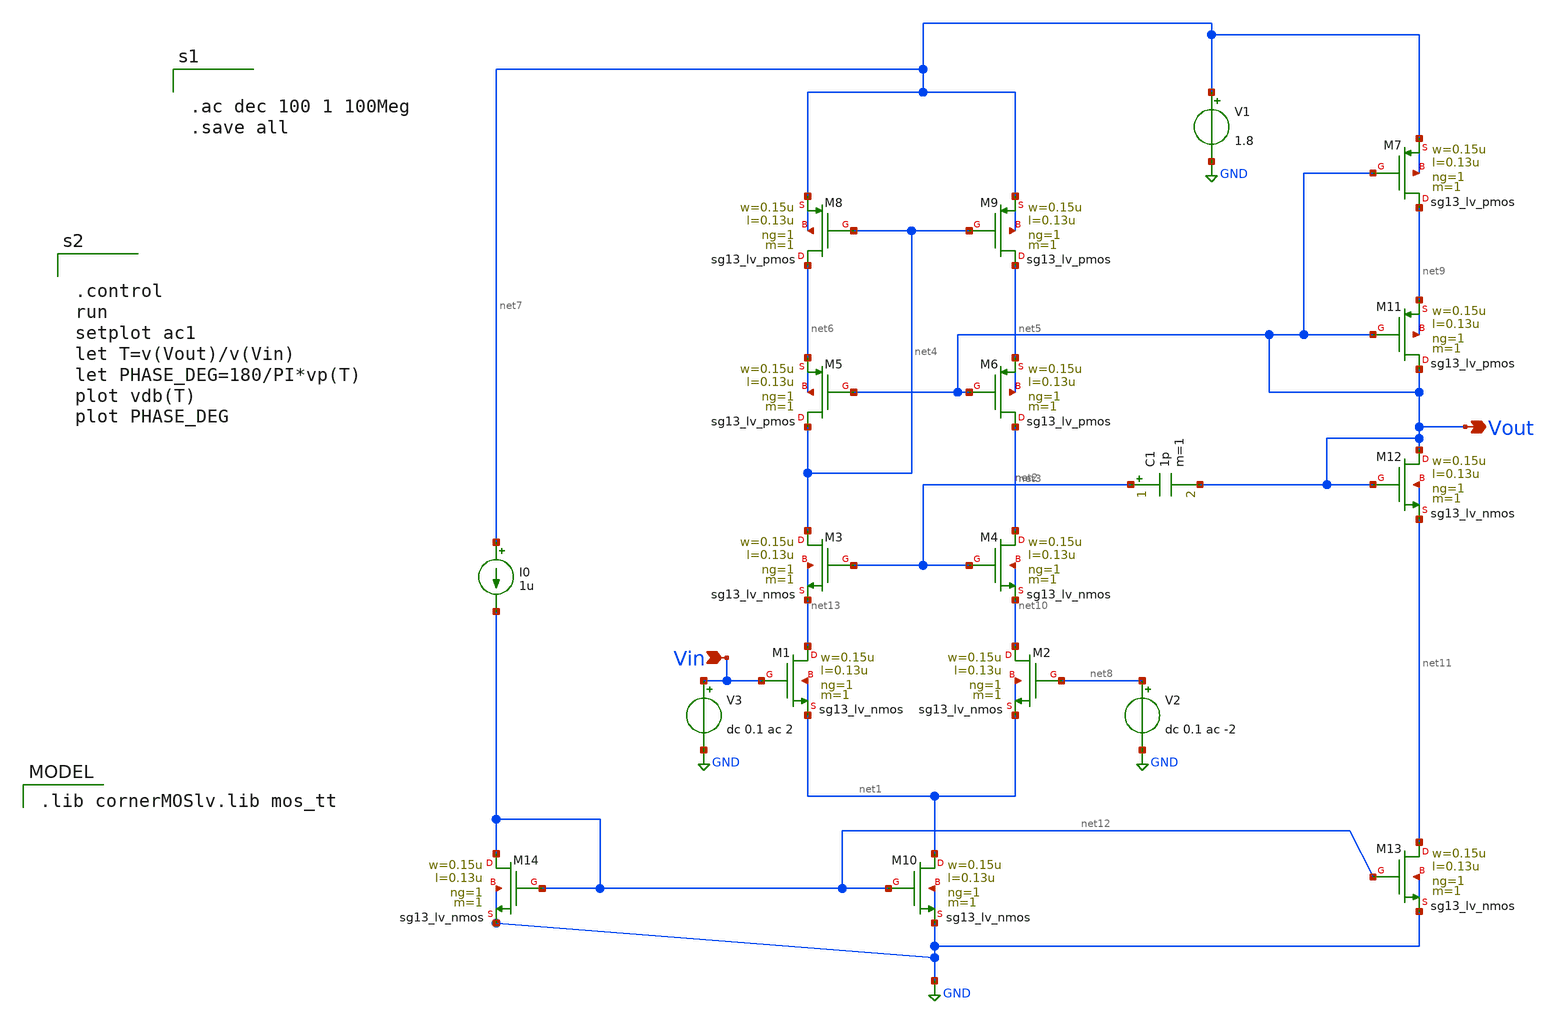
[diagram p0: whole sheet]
** sch_path: Telescopic_Twostage.sch
**.subckt Telescopic_Twostage Vin Vout
*.ipin Vin
*.opin Vout
XM1 net13 Vin net1 net1 sg13_lv_nmos w=0.15u l=0.13u ng=1 m=1 mm_ok=1
XM2 net10 net8 net1 net1 sg13_lv_nmos w=0.15u l=0.13u ng=1 m=1 mm_ok=1
XM3 net4 net2 net13 net13 sg13_lv_nmos w=0.15u l=0.13u ng=1 m=1 mm_ok=1
XM4 net3 net2 net10 net10 sg13_lv_nmos w=0.15u l=0.13u ng=1 m=1 mm_ok=1
XM5 net4 Vout net6 net6 sg13_lv_pmos w=0.15u l=0.13u ng=1 m=1 mm_ok=1
XM6 net3 Vout net5 net5 sg13_lv_pmos w=0.15u l=0.13u ng=1 m=1 mm_ok=1
XM8 net6 net4 net7 net7 sg13_lv_pmos w=0.15u l=0.13u ng=1 m=1 mm_ok=1
XM9 net5 net4 net7 net7 sg13_lv_pmos w=0.15u l=0.13u ng=1 m=1 mm_ok=1
XM10 net1 net12 GND GND sg13_lv_nmos w=0.15u l=0.13u ng=1 m=1 mm_ok=1
V1 net7 GND 1.8
V2 net8 GND dc 0.1 ac -2
V3 Vin GND dc 0.1 ac 2
XM7 net9 Vout net7 net7 sg13_lv_pmos w=0.15u l=0.13u ng=1 m=1 mm_ok=1
XM11 Vout Vout net9 net9 sg13_lv_pmos w=0.15u l=0.13u ng=1 m=1 mm_ok=1
XM12 Vout Vout net11 net11 sg13_lv_nmos w=0.15u l=0.13u ng=1 m=1 mm_ok=1
XM13 net11 net12 GND GND sg13_lv_nmos w=0.15u l=0.13u ng=1 m=1 mm_ok=1
XM14 net12 net12 GND GND sg13_lv_nmos w=0.15u l=0.13u ng=1 m=1 mm_ok=1
I0 net7 net12 1u
C1 net2 Vout 1p m=1
**** begin user architecture code


.ac dec 100 1 100Meg
.save all




.control
run
setplot ac1
let T=v(Vout)/v(Vin)
let PHASE_DEG=180/PI*vp(T)
plot vdb(T)
plot PHASE_DEG


 .lib cornerMOSlv.lib mos_tt

**** end user architecture code
**.ends
.GLOBAL GND
.end
